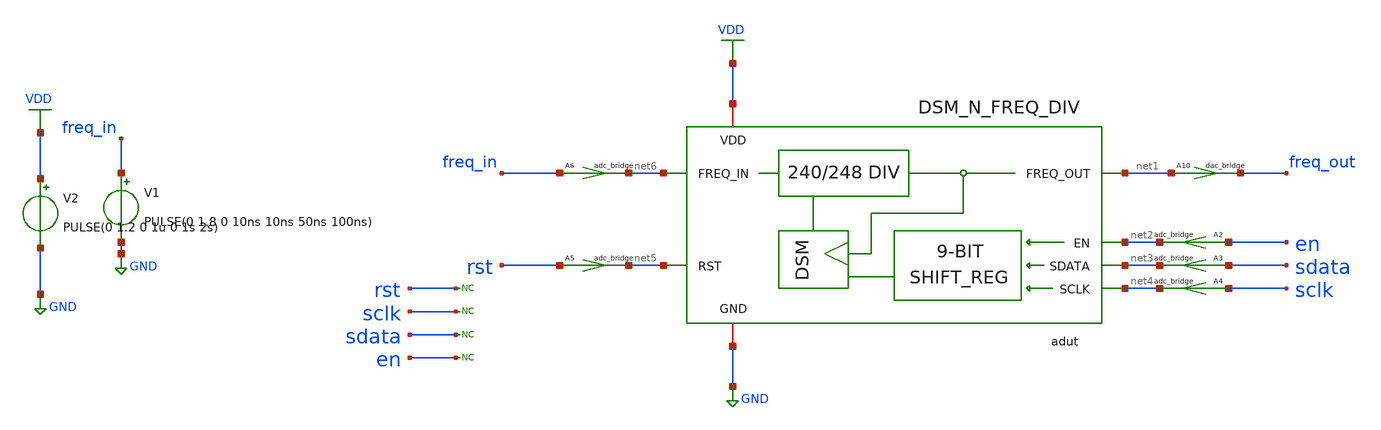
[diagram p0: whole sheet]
** sch_path: xschem/dsm/xschem/tb_DSM_N_FREQ_DIV.sch
* Copyright (C) 1998-2024 Stefan Frederik Schippers
* This program is free software; you can redistribute it and/or modify
* it under the terms of the GNU General Public License as published by
* the Free Software Foundation; either version 2 of the License, or
* (at your option) any later version.
* This program is distributed in the hope that it will be useful,
* but WITHOUT ANY WARRANTY; without even the implied warranty of
* MERCHANTABILITY or FITNESS FOR A PARTICULAR PURPOSE.  See the
* GNU General Public License for more details.
* You should have received a copy of the GNU General Public License
* along with this program; if not, write to the Free Software
**.subckt tb_DSM_N_FREQ_DIV
V1 freq_in GND PULSE(0 1.8 0 10ns 10ns 50ns 100ns)
A2 [ en ] [ net2 ] adc1
.model adc1 adc_bridge in_low=0.4 in_high=1.2
A3 [ sdata ] [ net3 ] adc1
.model adc1 adc_bridge in_low=0.4 in_high=1.2
A4 [ sclk ] [ net4 ] adc1
.model adc1 adc_bridge in_low=0.4 in_high=1.2
A5 [ rst ] [ net5 ] adc1
.model adc1 adc_bridge in_low=0.4 in_high=1.2
A6 [ freq_in ] [ net6 ] adc1
.model adc1 adc_bridge in_low=0.4 in_high=1.2
* noconn rst
* noconn sclk
* noconn sdata
* noconn en
A10 [ net1 ] [ freq_out ] dac1
.model dac1 dac_bridge out_low=0 out_high=1.2
adut [ net6 net5 net4 net3 net2 ] [ net1 ] null dut
.model dut d_cosim simulation=./../dsm_and_freq_divider.so
V2 VDD GND PULSE(0 1.2 0 1u 0 1s 2s)
**** begin user architecture code



* ngspice commands
.save v(dout) v(sdata) v(sclk) v(en) v(rst) v(dsm_clk) v(freq_in) v(freq_out)
.control
  tran 0.5n 1m
  remzerovec
  write tb_DSM_N_FREQ_DIV.raw
.endc

* to generate following file copy stimuli.test
* to the simulation directory and run simulation -> Utile Stimuli Editor (GUI),
* and press 'Translate'
.include stimuli_test.cir



**** end user architecture code
**.ends
.GLOBAL GND
.GLOBAL VDD
.end
